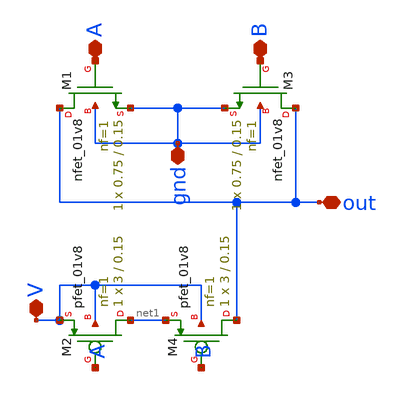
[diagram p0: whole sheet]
** sch_path: xschem/designs/counter4b/nor_gate.sch
**.subckt nor_gate A out gnd V B
*.iopin A
*.iopin out
*.iopin gnd
*.iopin V
*.iopin B
XM1 out A gnd gnd sky130_fd_pr__nfet_01v8 L=0.15 W=0.75 nf=1 ad='int((nf+1)/2) * W/nf * 0.29' as='int((nf+2)/2) * W/nf * 0.29'
+ pd='2*int((nf+1)/2) * (W/nf + 0.29)' ps='2*int((nf+2)/2) * (W/nf + 0.29)' nrd='0.29 / W' nrs='0.29 / W'
+ sa=0 sb=0 sd=0 mult=1 m=1
XM2 net1 A V V sky130_fd_pr__pfet_01v8 L=0.15 W=3 nf=1 ad='int((nf+1)/2) * W/nf * 0.29' as='int((nf+2)/2) * W/nf * 0.29'
+ pd='2*int((nf+1)/2) * (W/nf + 0.29)' ps='2*int((nf+2)/2) * (W/nf + 0.29)' nrd='0.29 / W' nrs='0.29 / W'
+ sa=0 sb=0 sd=0 mult=1 m=1
XM3 out B gnd gnd sky130_fd_pr__nfet_01v8 L=0.15 W=0.75 nf=1 ad='int((nf+1)/2) * W/nf * 0.29' as='int((nf+2)/2) * W/nf * 0.29'
+ pd='2*int((nf+1)/2) * (W/nf + 0.29)' ps='2*int((nf+2)/2) * (W/nf + 0.29)' nrd='0.29 / W' nrs='0.29 / W'
+ sa=0 sb=0 sd=0 mult=1 m=1
XM4 out B net1 V sky130_fd_pr__pfet_01v8 L=0.15 W=3 nf=1 ad='int((nf+1)/2) * W/nf * 0.29' as='int((nf+2)/2) * W/nf * 0.29'
+ pd='2*int((nf+1)/2) * (W/nf + 0.29)' ps='2*int((nf+2)/2) * (W/nf + 0.29)' nrd='0.29 / W' nrs='0.29 / W'
+ sa=0 sb=0 sd=0 mult=1 m=1
**.ends
.end
